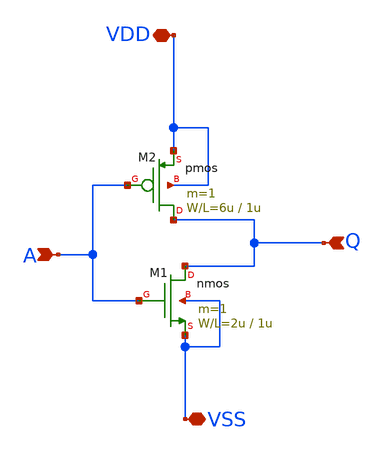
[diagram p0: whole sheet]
** sch_path: member_project/aidera/invertor_km_base.sch
**.subckt invertor_km_base Q A VSS VDD
*.ipin Q
*.ipin A
*.iopin VSS
*.iopin VDD
M1 Q A VSS VSS nmos L=1u W=2u m=1
M2 Q A VDD VDD pmos L=1u W=6u m=1
**.ends
.end
